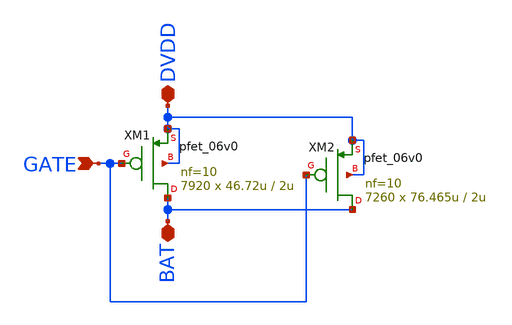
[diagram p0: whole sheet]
** sch_path: analog/xschem/power_fet_approx.sch
**.subckt power_fet_approx DVDD BAT GATE
*.iopin DVDD
*.iopin BAT
*.ipin GATE
XM1 BAT GATE DVDD DVDD pfet_06v0 L=2u W=46.72u nf=10 ad='int((nf+1)/2) * W/nf * 0.18u' as='int((nf+2)/2) * W/nf * 0.18u'
+ pd='2*int((nf+1)/2) * (W/nf + 0.18u)' ps='2*int((nf+2)/2) * (W/nf + 0.18u)' nrd='0.18u / W' nrs='0.18u / W'
+ sa=0 sb=0 sd=0 m=7920
XM2 BAT GATE DVDD DVDD pfet_06v0 L=2u W=76.465u nf=10 ad='int((nf+1)/2) * W/nf * 0.18u' as='int((nf+2)/2) * W/nf * 0.18u'
+ pd='2*int((nf+1)/2) * (W/nf + 0.18u)' ps='2*int((nf+2)/2) * (W/nf + 0.18u)' nrd='0.18u / W' nrs='0.18u / W'
+ sa=0 sb=0 sd=0 m=7260
**.ends
.end
